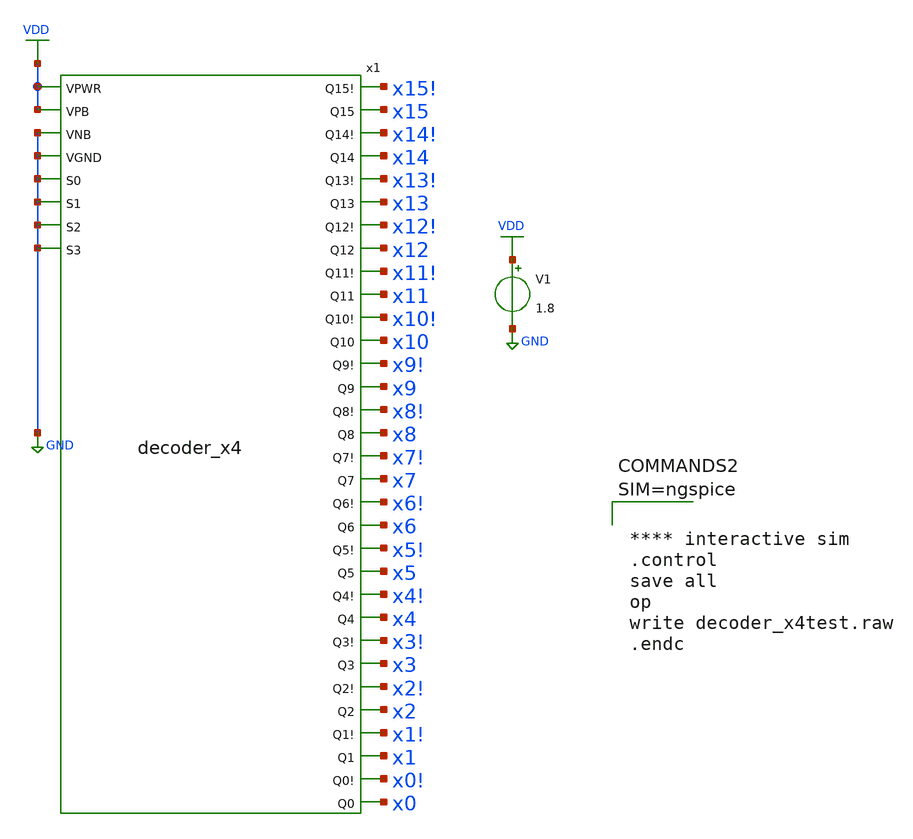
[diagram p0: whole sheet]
** sch_path: compiled 2/decoder_x4test.sch
**.subckt decoder_x4test
V1 VDD GND 1.8
x1 VDD VDD GND GND GND GND GND GND x15! x15 x14! x14 x13! x13 x12! x12 x11! x11 x10! x10 x9! x9 x8!
+ x8 x7! x7 x6! x6 x5! x5 x4! x4 x3! x3 x2! x2 x1! x1 x0! x0 decoder_x4
**** begin user architecture code

** opencircuitdesign pdks install
.lib $::SKYWATER_MODELS/sky130.lib.spice tt
.include $::SKYWATER_STDCELLS/sky130_fd_sc_hd.spice





**** interactive sim
.control
save all
op
write decoder_x4test.raw
.endc



**** end user architecture code
**.ends

* expanding   symbol:  decoder_x4.sym # of pins=40
** sym_path: compiled 2/decoder_x4.sym
** sch_path: compiled 2/decoder_x4.sch
.subckt decoder_x4 VPWR VPB VNB VGND S0 S1 S2 S3 Q15! Q15 Q14! Q14 Q13! Q13 Q12! Q12 Q11! Q11 Q10!
+ Q10 Q9! Q9 Q8! Q8 Q7! Q7 Q6! Q6 Q5! Q5 Q4! Q4 Q3! Q3 Q2! Q2 Q1! Q1 Q0! Q0
*.ipin S0
*.ipin S1
*.ipin S2
*.ipin S3
*.ipin VGND
*.ipin VPWR
*.ipin VNB
*.ipin VPB
*.opin Q14!
*.opin Q15!
*.opin Q13!
*.opin Q12!
*.opin Q10!
*.opin Q11!
*.opin Q9!
*.opin Q8!
*.opin Q7!
*.opin Q6!
*.opin Q4!
*.opin Q3!
*.opin Q2!
*.opin Q1!
*.opin Q0!
*.opin Q5!
*.opin Q14
*.opin Q15
*.opin Q13
*.opin Q12
*.opin Q10
*.opin Q11
*.opin Q9
*.opin Q8
*.opin Q7
*.opin Q6
*.opin Q4
*.opin Q3
*.opin Q2
*.opin Q1
*.opin Q0
*.opin Q5
x1 S0 S1 S2 S3 VGND VNB VPB VPWR Q15! sky130_fd_sc_hd__nand4_2
x2 S0 S1 S2 net1 VGND VNB VPB VPWR Q14! sky130_fd_sc_hd__nand4_2
x3 S0 S1 net2 S3 VGND VNB VPB VPWR Q13! sky130_fd_sc_hd__nand4_2
x4 S0 S1 net2 net1 VGND VNB VPB VPWR Q12! sky130_fd_sc_hd__nand4_2
x5 S0 net3 S2 S3 VGND VNB VPB VPWR Q11! sky130_fd_sc_hd__nand4_2
x6 S0 net3 S2 net1 VGND VNB VPB VPWR Q10! sky130_fd_sc_hd__nand4_2
x7 S0 net3 net2 S3 VGND VNB VPB VPWR Q9! sky130_fd_sc_hd__nand4_2
x8 S0 net3 net2 net1 VGND VNB VPB VPWR Q8! sky130_fd_sc_hd__nand4_2
x9 net4 S1 S2 S3 VGND VNB VPB VPWR Q7! sky130_fd_sc_hd__nand4_2
x10 net4 S1 S2 net1 VGND VNB VPB VPWR Q6! sky130_fd_sc_hd__nand4_2
x11 net4 S1 net2 S3 VGND VNB VPB VPWR Q5! sky130_fd_sc_hd__nand4_2
x12 net4 S1 net2 net1 VGND VNB VPB VPWR Q4! sky130_fd_sc_hd__nand4_2
x13 net4 net3 S2 S3 VGND VNB VPB VPWR Q3! sky130_fd_sc_hd__nand4_2
x14 net4 net3 S2 net1 VGND VNB VPB VPWR Q2! sky130_fd_sc_hd__nand4_2
x15 net4 net3 net2 S3 VGND VNB VPB VPWR Q1! sky130_fd_sc_hd__nand4_2
x16 net4 net3 net2 net1 VGND VNB VPB VPWR Q0! sky130_fd_sc_hd__nand4_2
x17 S0 VGND VNB VPB VPWR net4 sky130_fd_sc_hd__inv_8
x18 S1 VGND VNB VPB VPWR net3 sky130_fd_sc_hd__inv_8
x19 S2 VGND VNB VPB VPWR net2 sky130_fd_sc_hd__inv_8
x20 S3 VGND VNB VPB VPWR net1 sky130_fd_sc_hd__inv_8
x21 Q15! VGND VNB VPB VPWR Q15 sky130_fd_sc_hd__inv_1
x22 Q14! VGND VNB VPB VPWR Q14 sky130_fd_sc_hd__inv_1
x23 Q13! VGND VNB VPB VPWR Q13 sky130_fd_sc_hd__inv_1
x24 Q12! VGND VNB VPB VPWR Q12 sky130_fd_sc_hd__inv_1
x25 Q11! VGND VNB VPB VPWR Q11 sky130_fd_sc_hd__inv_1
x26 Q10! VGND VNB VPB VPWR Q10 sky130_fd_sc_hd__inv_1
x27 Q9! VGND VNB VPB VPWR Q9 sky130_fd_sc_hd__inv_1
x28 Q8! VGND VNB VPB VPWR Q8 sky130_fd_sc_hd__inv_1
x29 Q7! VGND VNB VPB VPWR Q7 sky130_fd_sc_hd__inv_1
x30 Q6! VGND VNB VPB VPWR Q6 sky130_fd_sc_hd__inv_1
x31 Q5! VGND VNB VPB VPWR Q5 sky130_fd_sc_hd__inv_1
x32 Q4! VGND VNB VPB VPWR Q4 sky130_fd_sc_hd__inv_1
x33 Q3! VGND VNB VPB VPWR Q3 sky130_fd_sc_hd__inv_1
x34 Q2! VGND VNB VPB VPWR Q2 sky130_fd_sc_hd__inv_1
x35 Q1! VGND VNB VPB VPWR Q1 sky130_fd_sc_hd__inv_1
x36 Q0! VGND VNB VPB VPWR Q0 sky130_fd_sc_hd__inv_1
.ends

.GLOBAL VDD
.GLOBAL GND
.end
